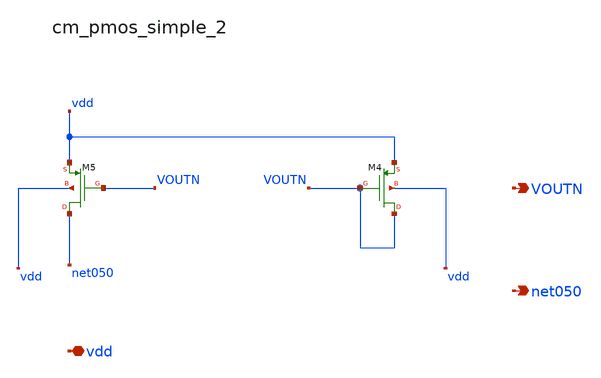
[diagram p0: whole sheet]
** sch_path: analog-db/raw/amp_013_qu2017_azc/hier/blocks/cm_pmos_simple_2.sch
**.subckt cm_pmos_simple_2 vdd VOUTN net050
*.iopin vdd
*.opin VOUTN
*.opin net050
XM4 VOUTN VOUTN vdd vdd sg13_lv_pmos w=x_dut_xm4_w l=x_dut_xm4_l ng=1 m=x_dut_xm4_m
XM5 net050 VOUTN vdd vdd sg13_lv_pmos w=x_dut_xm5_w l=x_dut_xm5_l ng=1 m=x_dut_xm5_m
**.ends
.end
